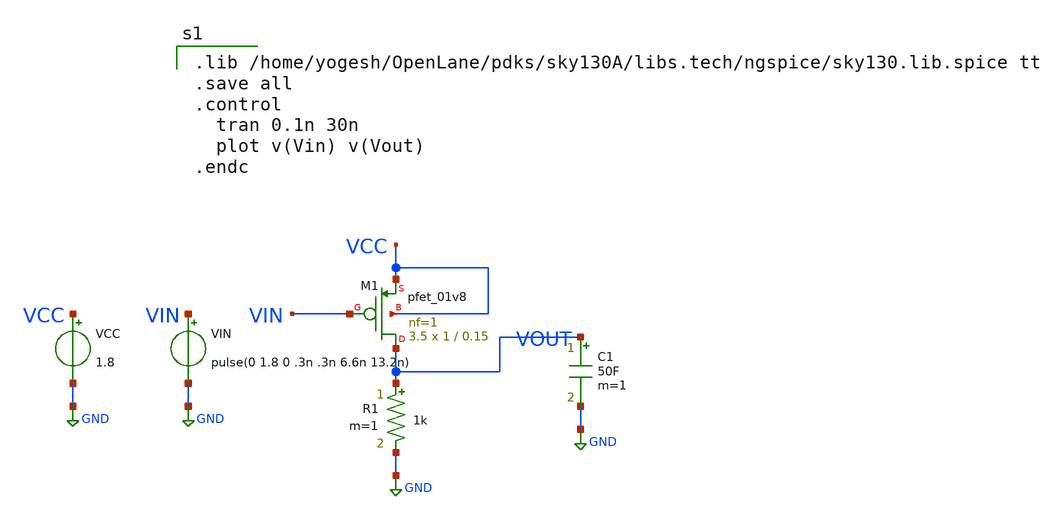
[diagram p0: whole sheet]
** sch_path: OneDrive/Documents/CMOS-Inverter-Design-and-Analysis-using-Sky130pdk-main/xschem/pmos_invF.sch
**.subckt pmos_invF
VIN VIN GND pulse(0 1.8 0 .3n .3n 6.6n 13.2n)
VCC VCC GND 1.8
R1 VOUT GND 1k m=1
C1 VOUT GND 50F m=1
XM1 VOUT VIN VCC VCC sky130_fd_pr__pfet_01v8 L=0.15 W=1 nf=1 ad='int((nf+1)/2) * W/nf * 0.29' as='int((nf+2)/2) * W/nf * 0.29'
+ pd='2*int((nf+1)/2) * (W/nf + 0.29)' ps='2*int((nf+2)/2) * (W/nf + 0.29)' nrd='0.29 / W' nrs='0.29 / W'
+ sa=0 sb=0 sd=0 mult=3.5 m=3.5
**** begin user architecture code

.lib /home/yogesh/OpenLane/pdks/sky130A/libs.tech/ngspice/sky130.lib.spice tt
.save all
.control
  tran 0.1n 30n
  plot v(Vin) v(Vout)
.endc

**** end user architecture code
**.ends
.GLOBAL GND
.end
